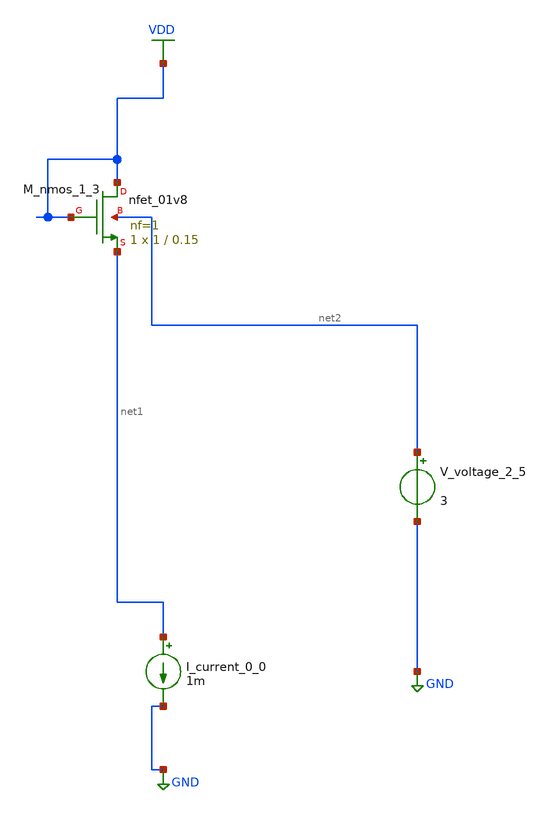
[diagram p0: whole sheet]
** sch_path: schematics/AMSNet/38.sch
**.subckt 38
I_current_0_0 net1 GND 1m
XM_nmos_1_3 VDD VDD net1 net2 sky130_fd_pr__nfet_01v8 L=0.15 W=1 nf=1 ad='int((1 + 1)/2) * 1 / 1 * 0.29'
+ as='int((1 + 2)/2) * 1 / 1 * 0.29' pd='2*int((1 + 1)/2) * (1 / 1 + 0.29)' ps='2*int((1 + 2)/2) * (1 / 1 + 0.29)'
+ nrd='0.29 / 1 ' nrs='0.29 / 1 ' sa=0 sb=0 sd=0 mult=1 m=1
V_voltage_2_5 net2 GND 3
**.ends
.GLOBAL GND
.GLOBAL VDD
.end
